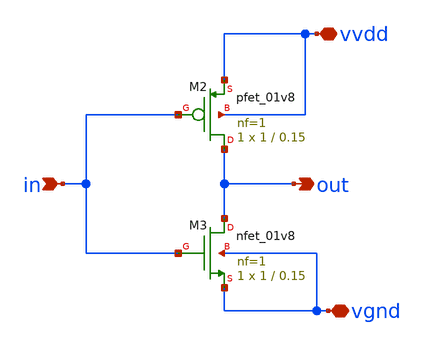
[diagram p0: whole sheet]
** sch_path: inverter.sch
**.subckt inverter vvdd vgnd in out
*.iopin vvdd
*.iopin vgnd
*.ipin in
*.opin out
XM2 out in vvdd vvdd sky130_fd_pr__pfet_01v8 L=0.15 W=1 nf=1 ad='int((nf+1)/2) * W/nf * 0.29' as='int((nf+2)/2) * W/nf * 0.29'
+ pd='2*int((nf+1)/2) * (W/nf + 0.29)' ps='2*int((nf+2)/2) * (W/nf + 0.29)' nrd='0.29 / W' nrs='0.29 / W'
+ sa=0 sb=0 sd=0 mult=1 m=1
XM3 out in vgnd vgnd sky130_fd_pr__nfet_01v8 L=0.15 W=1 nf=1 ad='int((nf+1)/2) * W/nf * 0.29' as='int((nf+2)/2) * W/nf * 0.29'
+ pd='2*int((nf+1)/2) * (W/nf + 0.29)' ps='2*int((nf+2)/2) * (W/nf + 0.29)' nrd='0.29 / W' nrs='0.29 / W'
+ sa=0 sb=0 sd=0 mult=1 m=1
**.ends
.end
